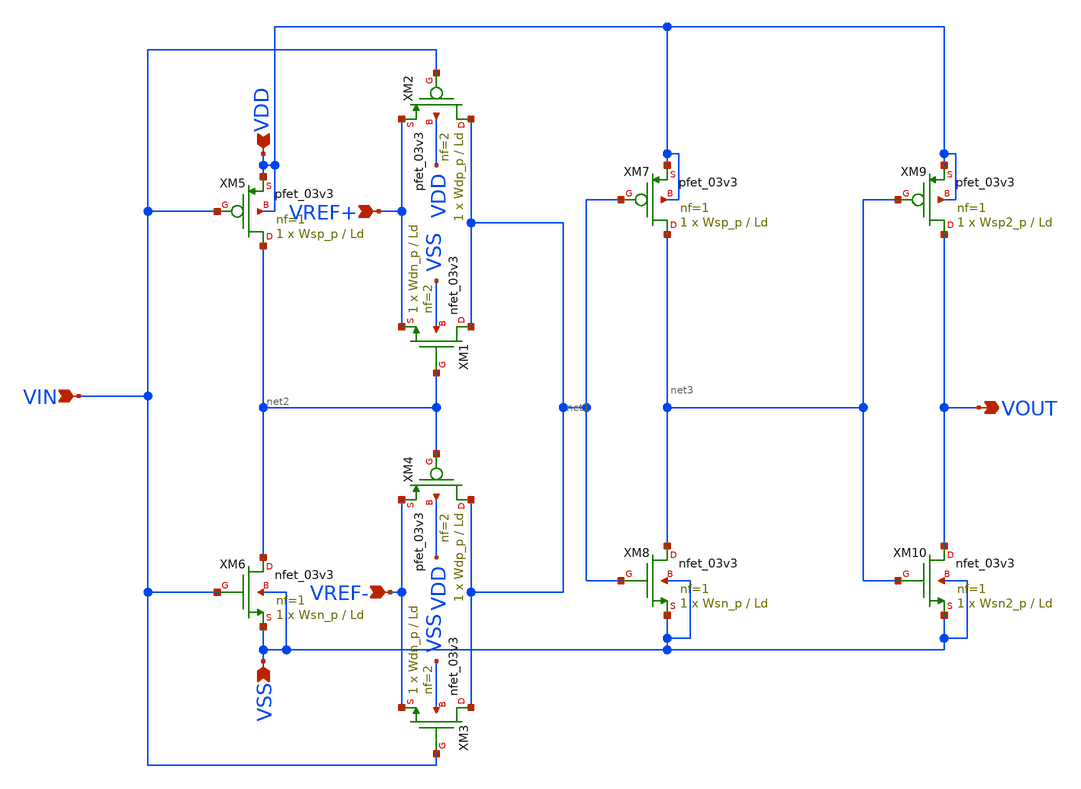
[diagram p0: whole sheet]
** sch_path: src/schematics/dac_1bit/DAC_1_BIT_PLUS.sch
**.subckt DAC_1_BIT_PLUS VIN VREF+ VREF- VOUT VDD VSS
*.ipin VIN
*.ipin VREF+
*.ipin VREF-
*.opin VOUT
*.ipin VDD
*.ipin VSS
XM1 net1 net2 VREF+ VSS nfet_03v3 L=Ld W=Wdn_p nf=2 ad='int((nf+1)/2) * W/nf * 0.18u' as='int((nf+2)/2) * W/nf * 0.18u'
+ pd='2*int((nf+1)/2) * (W/nf + 0.18u)' ps='2*int((nf+2)/2) * (W/nf + 0.18u)' nrd='0.18u / W' nrs='0.18u / W'
+ sa=0 sb=0 sd=0 m=1
XM2 net1 VIN VREF+ VDD pfet_03v3 L=Ld W=Wdp_p nf=2 ad='int((nf+1)/2) * W/nf * 0.18u' as='int((nf+2)/2) * W/nf * 0.18u'
+ pd='2*int((nf+1)/2) * (W/nf + 0.18u)' ps='2*int((nf+2)/2) * (W/nf + 0.18u)' nrd='0.18u / W' nrs='0.18u / W'
+ sa=0 sb=0 sd=0 m=1
XM3 net1 VIN VREF- VSS nfet_03v3 L=Ld W=Wdn_p nf=2 ad='int((nf+1)/2) * W/nf * 0.18u' as='int((nf+2)/2) * W/nf * 0.18u'
+ pd='2*int((nf+1)/2) * (W/nf + 0.18u)' ps='2*int((nf+2)/2) * (W/nf + 0.18u)' nrd='0.18u / W' nrs='0.18u / W'
+ sa=0 sb=0 sd=0 m=1
XM4 net1 net2 VREF- VDD pfet_03v3 L=Ld W=Wdp_p nf=2 ad='int((nf+1)/2) * W/nf * 0.18u' as='int((nf+2)/2) * W/nf * 0.18u'
+ pd='2*int((nf+1)/2) * (W/nf + 0.18u)' ps='2*int((nf+2)/2) * (W/nf + 0.18u)' nrd='0.18u / W' nrs='0.18u / W'
+ sa=0 sb=0 sd=0 m=1
XM5 net2 VIN VDD VDD pfet_03v3 L=Ld W=Wsp_p nf=1 ad='int((nf+1)/2) * W/nf * 0.18u' as='int((nf+2)/2) * W/nf * 0.18u'
+ pd='2*int((nf+1)/2) * (W/nf + 0.18u)' ps='2*int((nf+2)/2) * (W/nf + 0.18u)' nrd='0.18u / W' nrs='0.18u / W'
+ sa=0 sb=0 sd=0 m=1
XM6 net2 VIN VSS VSS nfet_03v3 L=Ld W=Wsn_p nf=1 ad='int((nf+1)/2) * W/nf * 0.18u' as='int((nf+2)/2) * W/nf * 0.18u'
+ pd='2*int((nf+1)/2) * (W/nf + 0.18u)' ps='2*int((nf+2)/2) * (W/nf + 0.18u)' nrd='0.18u / W' nrs='0.18u / W'
+ sa=0 sb=0 sd=0 m=1
XM7 net3 net1 VDD VDD pfet_03v3 L=Ld W=Wsp_p nf=1 ad='int((nf+1)/2) * W/nf * 0.18u' as='int((nf+2)/2) * W/nf * 0.18u'
+ pd='2*int((nf+1)/2) * (W/nf + 0.18u)' ps='2*int((nf+2)/2) * (W/nf + 0.18u)' nrd='0.18u / W' nrs='0.18u / W'
+ sa=0 sb=0 sd=0 m=1
XM8 net3 net1 VSS VSS nfet_03v3 L=Ld W=Wsn_p nf=1 ad='int((nf+1)/2) * W/nf * 0.18u' as='int((nf+2)/2) * W/nf * 0.18u'
+ pd='2*int((nf+1)/2) * (W/nf + 0.18u)' ps='2*int((nf+2)/2) * (W/nf + 0.18u)' nrd='0.18u / W' nrs='0.18u / W'
+ sa=0 sb=0 sd=0 m=1
XM9 VOUT net3 VDD VDD pfet_03v3 L=Ld W=Wsp2_p nf=1 ad='int((nf+1)/2) * W/nf * 0.18u' as='int((nf+2)/2) * W/nf * 0.18u'
+ pd='2*int((nf+1)/2) * (W/nf + 0.18u)' ps='2*int((nf+2)/2) * (W/nf + 0.18u)' nrd='0.18u / W' nrs='0.18u / W'
+ sa=0 sb=0 sd=0 m=1
XM10 VOUT net3 VSS VSS nfet_03v3 L=Ld W=Wsn2_p nf=1 ad='int((nf+1)/2) * W/nf * 0.18u' as='int((nf+2)/2) * W/nf * 0.18u'
+ pd='2*int((nf+1)/2) * (W/nf + 0.18u)' ps='2*int((nf+2)/2) * (W/nf + 0.18u)' nrd='0.18u / W' nrs='0.18u / W'
+ sa=0 sb=0 sd=0 m=1
**.ends
.end
